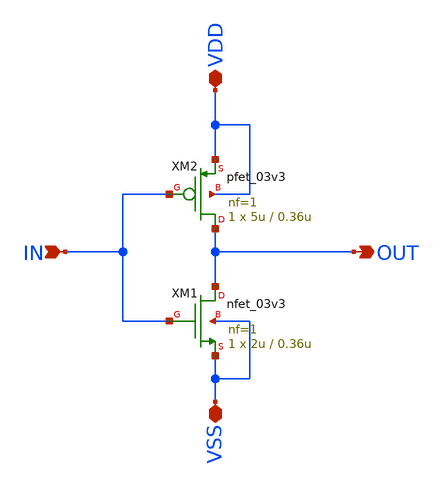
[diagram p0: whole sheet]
** sch_path: Array Components/Switch Array/CMOS Inverter/inv2.sch
**.subckt inv2 VDD VSS IN OUT
*.iopin VDD
*.iopin VSS
*.ipin IN
*.opin OUT
XM1 OUT IN VSS VSS nfet_03v3 L=0.36u W=2u nf=1 ad='int((nf+1)/2) * W/nf * 0.18u' as='int((nf+2)/2) * W/nf * 0.18u'
+ pd='2*int((nf+1)/2) * (W/nf + 0.18u)' ps='2*int((nf+2)/2) * (W/nf + 0.18u)' nrd='0.18u / W' nrs='0.18u / W'
+ sa=0 sb=0 sd=0 m=1
XM2 OUT IN VDD VDD pfet_03v3 L=0.36u W=5u nf=1 ad='int((nf+1)/2) * W/nf * 0.18u' as='int((nf+2)/2) * W/nf * 0.18u'
+ pd='2*int((nf+1)/2) * (W/nf + 0.18u)' ps='2*int((nf+2)/2) * (W/nf + 0.18u)' nrd='0.18u / W' nrs='0.18u / W'
+ sa=0 sb=0 sd=0 m=1
**.ends
.end
